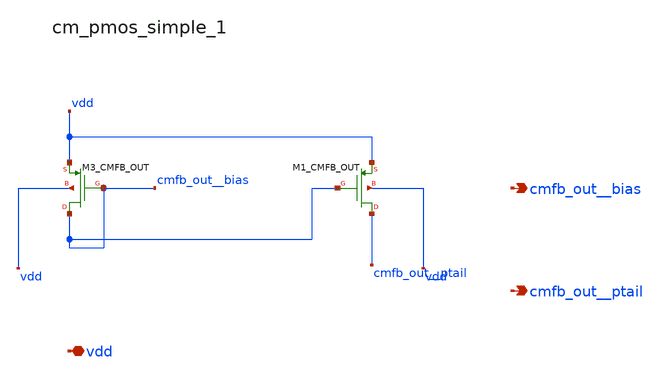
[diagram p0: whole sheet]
** sch_path: analog-db/raw/amp_035_fan_chopper_cmfb_dual/hier/blocks/cm_pmos_simple_1.sch
**.subckt cm_pmos_simple_1 vdd cmfb_out__bias cmfb_out__ptail
*.iopin vdd
*.opin cmfb_out__bias
*.opin cmfb_out__ptail
XM1_CMFB_OUT cmfb_out__ptail cmfb_out__bias vdd vdd sg13_lv_pmos w=x_dut_xm1_cmfb_out_w
+ l=x_dut_xm1_cmfb_out_l ng=1 m=x_dut_xm1_cmfb_out_m
XM3_CMFB_OUT cmfb_out__bias cmfb_out__bias vdd vdd sg13_lv_pmos w=x_dut_xm3_cmfb_out_w
+ l=x_dut_xm3_cmfb_out_l ng=1 m=x_dut_xm3_cmfb_out_m
**.ends
.end
